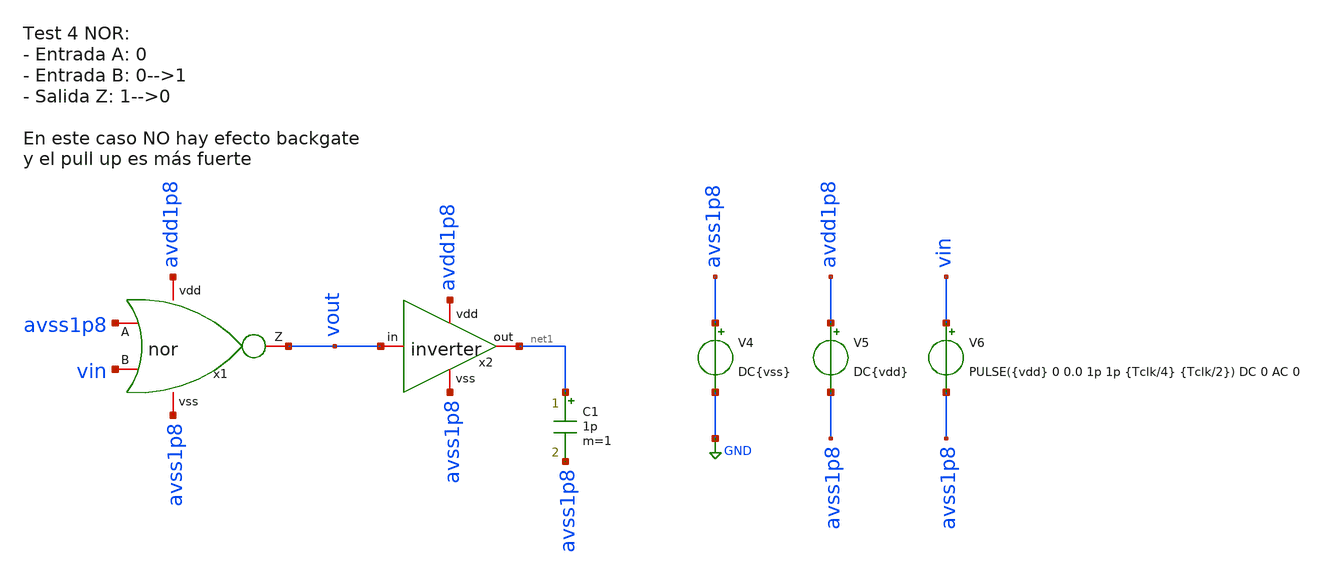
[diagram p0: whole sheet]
** sch_path: designs/sch/tests/test4_nor.sch
**.subckt test4_nor
x2 avdd1p8 net1 vout avss1p8 inverter
V4 avss1p8 GND DC{vss}
V5 avdd1p8 avss1p8 DC{vdd}
V6 vin avss1p8 PULSE({vdd} 0 0.0 1p 1p {Tclk/4} {Tclk/2}) DC 0 AC 0
C1 net1 avss1p8 1p m=1
x1 avdd1p8 vout avss1p8 vin avss1p8 nor
**** begin user architecture code


* Circuit Parameters
.param vdd = 1.8
.param vss = 0.0
.param Tclk = 10n
.options TEMP = 65.0

* Include Models
.lib /foss/pdks/sky130A/libs.tech/ngspice/sky130.lib.spice TT

* OP Parameters & Singals to save
.save all

* Simulations
.control
  tran 0.01u 100n
  setplot tran1
  plot v(vin) v(vout)+2
reset
  dc V6 0 1.8 0.01
  setplot dc
  plot vin vout ylabel vout xlabel vin
  set filetype = ascii
  write dcsweep.raw
.endc

.end


**** end user architecture code
**.ends

* expanding   symbol:  /foss/designs/sch/inverter.sym # of pins=4
** sym_path: designs/inverter.sym
** sch_path: designs/inverter.sch
.subckt inverter vdd out in vss
*.iopin out
*.iopin vss
*.iopin vdd
*.iopin in
XM2 out in vss vss sky130_fd_pr__nfet_01v8 L=0.15 W=0.75 nf=1 ad='int((nf+1)/2) * W/nf * 0.29' as='int((nf+2)/2) * W/nf * 0.29'
+ pd='2*int((nf+1)/2) * (W/nf + 0.29)' ps='2*int((nf+2)/2) * (W/nf + 0.29)' nrd='0.29 / W' nrs='0.29 / W'
+ sa=0 sb=0 sd=0 mult=1 m=1
XM1 out in vdd vdd sky130_fd_pr__pfet_01v8 L=0.15 W=1.5 nf=1 ad='int((nf+1)/2) * W/nf * 0.29' as='int((nf+2)/2) * W/nf * 0.29'
+ pd='2*int((nf+1)/2) * (W/nf + 0.29)' ps='2*int((nf+2)/2) * (W/nf + 0.29)' nrd='0.29 / W' nrs='0.29 / W'
+ sa=0 sb=0 sd=0 mult=1 m=1
.ends


* expanding   symbol:  /foss/designs/sch/nor.sym # of pins=5
** sym_path: designs/sch/nor.sym
** sch_path: designs/sch/nor.sch
.subckt nor vdd Z A B vss
*.iopin A
*.iopin B
*.iopin vdd
*.iopin Z
*.iopin vss
XM1 Z A vss vss sky130_fd_pr__nfet_01v8 L=0.15 W=0.75 nf=1 ad='int((nf+1)/2) * W/nf * 0.29' as='int((nf+2)/2) * W/nf * 0.29'
+ pd='2*int((nf+1)/2) * (W/nf + 0.29)' ps='2*int((nf+2)/2) * (W/nf + 0.29)' nrd='0.29 / W' nrs='0.29 / W'
+ sa=0 sb=0 sd=0 mult=1 m=1
XM4 net1 B vdd vdd sky130_fd_pr__pfet_01v8 L=0.15 W=3 nf=1 ad='int((nf+1)/2) * W/nf * 0.29' as='int((nf+2)/2) * W/nf * 0.29'
+ pd='2*int((nf+1)/2) * (W/nf + 0.29)' ps='2*int((nf+2)/2) * (W/nf + 0.29)' nrd='0.29 / W' nrs='0.29 / W'
+ sa=0 sb=0 sd=0 mult=1 m=1
XM2 Z B vss vss sky130_fd_pr__nfet_01v8 L=0.15 W=0.75 nf=1 ad='int((nf+1)/2) * W/nf * 0.29' as='int((nf+2)/2) * W/nf * 0.29'
+ pd='2*int((nf+1)/2) * (W/nf + 0.29)' ps='2*int((nf+2)/2) * (W/nf + 0.29)' nrd='0.29 / W' nrs='0.29 / W'
+ sa=0 sb=0 sd=0 mult=1 m=1
XM3 Z A net1 vdd sky130_fd_pr__pfet_01v8 L=0.15 W=3 nf=1 ad='int((nf+1)/2) * W/nf * 0.29' as='int((nf+2)/2) * W/nf * 0.29'
+ pd='2*int((nf+1)/2) * (W/nf + 0.29)' ps='2*int((nf+2)/2) * (W/nf + 0.29)' nrd='0.29 / W' nrs='0.29 / W'
+ sa=0 sb=0 sd=0 mult=1 m=1
.ends

.GLOBAL GND
.end
